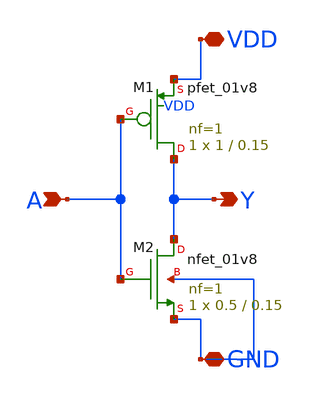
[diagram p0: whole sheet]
** sch_path: schematic/inv.sch
**.subckt inv VDD GND A Y
*.iopin VDD
*.iopin GND
*.ipin A
*.opin Y
XM1 Y A VDD VDD sky130_fd_pr__pfet_01v8 L=0.15 W=1 nf=1 ad='int((1 + 1)/2) * 1 / 1 * 0.29' as='int((1 + 2)/2) * 1 / 1 * 0.29'
+ pd='2*int((1 + 1)/2) * (1 / 1 + 0.29)' ps='2*int((1 + 2)/2) * (1 / 1 + 0.29)' nrd='0.29 / 1 ' nrs='0.29 / 1 '
+ sa=0 sb=0 sd=0 mult=1 m=1
XM2 Y A GND GND sky130_fd_pr__nfet_01v8 L=0.15 W=0.5 nf=1 ad='int((1 + 1)/2) * 0.5 / 1 * 0.29' as='int((1 + 2)/2) * 0.5 / 1 * 0.29'
+ pd='2*int((1 + 1)/2) * (0.5 / 1 + 0.29)' ps='2*int((1 + 2)/2) * (0.5 / 1 + 0.29)' nrd='0.29 / 0.5 ' nrs='0.29 / 0.5 '
+ sa=0 sb=0 sd=0 mult=1 m=1
**.ends
.end
